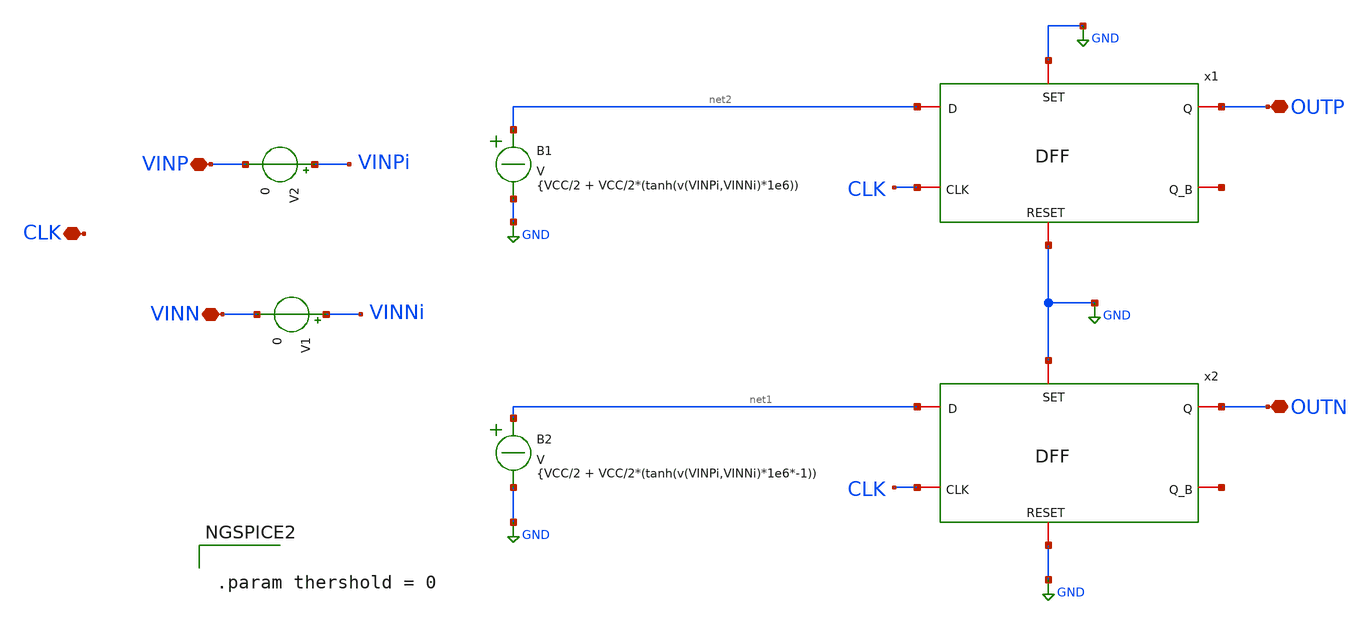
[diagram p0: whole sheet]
** sch_path: Designs/comp.sch
**.subckt comp VINP VINN CLK OUTP OUTN
*.iopin VINP
*.iopin VINN
*.iopin CLK
*.iopin OUTP
*.iopin OUTN
V1 VINNi VINN 0
V2 VINPi VINP 0
B1 net2 GND V = {VCC/2 + VCC/2*(tanh(v(VINPi,VINNi)*1e6))
B2 net1 GND V = {VCC/2 + VCC/2*(tanh(v(VINPi,VINNi)*1e6*-1))
x1 net2 CLK GND OUTP net3 GND DFF
x2 net1 CLK GND OUTN net4 GND DFF
**** begin user architecture code


.param thershold = 0


**** end user architecture code
**.ends
.GLOBAL GND
.end
